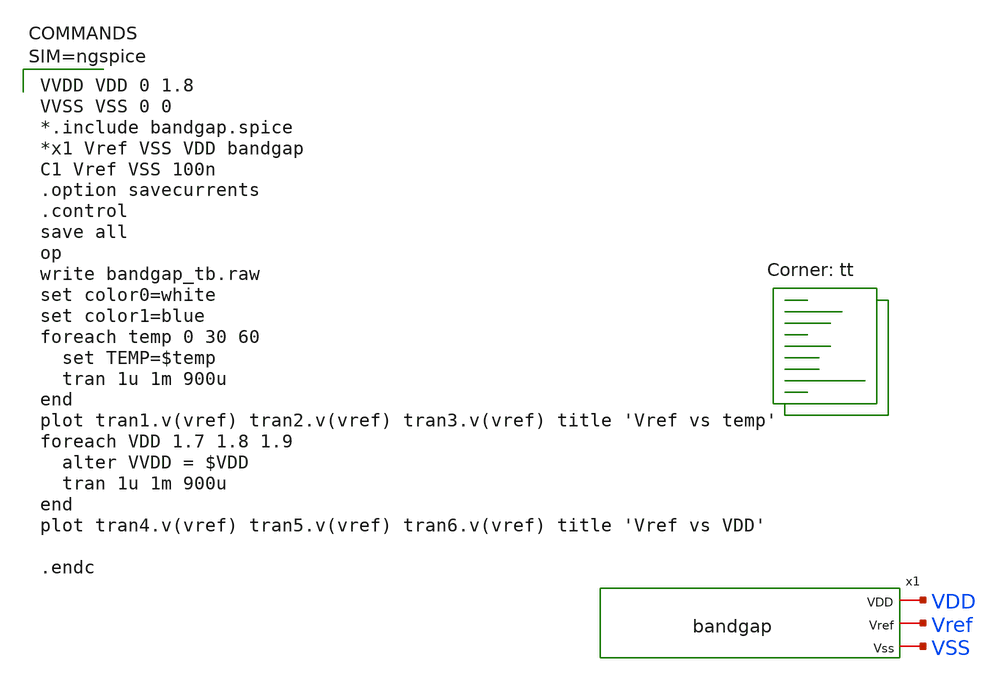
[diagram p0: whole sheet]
** sch_path: hw05/xschem/bandgap_tb.sch
**.subckt bandgap_tb
x1 VDD Vref VSS bandgap
**** begin user architecture code
.lib $::SKYWATER_MODELS/sky130.lib.spice tt


VVDD VDD 0 1.8
VVSS VSS 0 0
*.include bandgap.spice
*x1 Vref VSS VDD bandgap
C1 Vref VSS 100n
.option savecurrents
.control
save all
op
write bandgap_tb.raw
set color0=white
set color1=blue
foreach temp 0 30 60
  set TEMP=$temp
  tran 1u 1m 900u
end
plot tran1.v(vref) tran2.v(vref) tran3.v(vref) title 'Vref vs temp'
foreach VDD 1.7 1.8 1.9
  alter VVDD = $VDD
  tran 1u 1m 900u
end
plot tran4.v(vref) tran5.v(vref) tran6.v(vref) title 'Vref vs VDD'

.endc



**** end user architecture code
**.ends

* expanding   symbol:  bandgap.sym # of pins=3
** sym_path: hw05/xschem/bandgap.sym
** sch_path: hw05/xschem/bandgap.sch
.subckt bandgap VDD Vref Vss
*.iopin VDD
*.iopin Vss
*.iopin Vref
XM7 net2 Vref net8 Vss sky130_fd_pr__nfet_01v8 L=1 W=20 nf=1 ad='int((nf+1)/2) * W/nf * 0.29' as='int((nf+2)/2) * W/nf * 0.29'
+ pd='2*int((nf+1)/2) * (W/nf + 0.29)' ps='2*int((nf+2)/2) * (W/nf + 0.29)' nrd='0.29 / W' nrs='0.29 / W'
+ sa=0 sb=0 sd=0 mult=1 m=1
XM1 net1 net1 VDD VDD sky130_fd_pr__pfet_01v8 L=1 W=1 nf=1 ad='int((nf+1)/2) * W/nf * 0.29' as='int((nf+2)/2) * W/nf * 0.29'
+ pd='2*int((nf+1)/2) * (W/nf + 0.29)' ps='2*int((nf+2)/2) * (W/nf + 0.29)' nrd='0.29 / W' nrs='0.29 / W'
+ sa=0 sb=0 sd=0 mult=1 m=1
XM2 net2 net1 VDD VDD sky130_fd_pr__pfet_01v8 L=1 W=1 nf=1 ad='int((nf+1)/2) * W/nf * 0.29' as='int((nf+2)/2) * W/nf * 0.29'
+ pd='2*int((nf+1)/2) * (W/nf + 0.29)' ps='2*int((nf+2)/2) * (W/nf + 0.29)' nrd='0.29 / W' nrs='0.29 / W'
+ sa=0 sb=0 sd=0 mult=1 m=1
XM3 net5 net1 VDD VDD sky130_fd_pr__pfet_01v8 L=1 W=1 nf=1 ad='int((nf+1)/2) * W/nf * 0.29' as='int((nf+2)/2) * W/nf * 0.29'
+ pd='2*int((nf+1)/2) * (W/nf + 0.29)' ps='2*int((nf+2)/2) * (W/nf + 0.29)' nrd='0.29 / W' nrs='0.29 / W'
+ sa=0 sb=0 sd=0 mult=1 m=1
XM4 Vref net2 VDD VDD sky130_fd_pr__pfet_01v8 L=.5 W=20 nf=1 ad='int((nf+1)/2) * W/nf * 0.29' as='int((nf+2)/2) * W/nf * 0.29'
+ pd='2*int((nf+1)/2) * (W/nf + 0.29)' ps='2*int((nf+2)/2) * (W/nf + 0.29)' nrd='0.29 / W' nrs='0.29 / W'
+ sa=0 sb=0 sd=0 mult=1 m=1
XM5 net1 Vref net4 Vss sky130_fd_pr__nfet_01v8 L=1 W=5 nf=1 ad='int((nf+1)/2) * W/nf * 0.29' as='int((nf+2)/2) * W/nf * 0.29'
+ pd='2*int((nf+1)/2) * (W/nf + 0.29)' ps='2*int((nf+2)/2) * (W/nf + 0.29)' nrd='0.29 / W' nrs='0.29 / W'
+ sa=0 sb=0 sd=0 mult=1 m=1
XR1 net3 net4 Vss sky130_fd_pr__res_xhigh_po_5p73 L=80 mult=1 m=1
XR2 Vss net3 Vss sky130_fd_pr__res_xhigh_po_5p73 L=80 mult=1 m=1
XM6 net9 net2 Vss Vss sky130_fd_pr__nfet_01v8 L=50 W=.42 nf=1 ad='int((nf+1)/2) * W/nf * 0.29' as='int((nf+2)/2) * W/nf * 0.29'
+ pd='2*int((nf+1)/2) * (W/nf + 0.29)' ps='2*int((nf+2)/2) * (W/nf + 0.29)' nrd='0.29 / W' nrs='0.29 / W'
+ sa=0 sb=0 sd=0 mult=1 m=1
XM8 net8 net7 Vss Vss sky130_fd_pr__nfet_01v8 L=1 W=20 nf=1 ad='int((nf+1)/2) * W/nf * 0.29' as='int((nf+2)/2) * W/nf * 0.29'
+ pd='2*int((nf+1)/2) * (W/nf + 0.29)' ps='2*int((nf+2)/2) * (W/nf + 0.29)' nrd='0.29 / W' nrs='0.29 / W'
+ sa=0 sb=0 sd=0 mult=1 m=1
XM9 net7 net6 Vss Vss sky130_fd_pr__nfet_01v8 L=1 W=20 nf=1 ad='int((nf+1)/2) * W/nf * 0.29' as='int((nf+2)/2) * W/nf * 0.29'
+ pd='2*int((nf+1)/2) * (W/nf + 0.29)' ps='2*int((nf+2)/2) * (W/nf + 0.29)' nrd='0.29 / W' nrs='0.29 / W'
+ sa=0 sb=0 sd=0 mult=1 m=1
XM10 net6 net6 Vss Vss sky130_fd_pr__nfet_01v8 L=1 W=20 nf=1 ad='int((nf+1)/2) * W/nf * 0.29' as='int((nf+2)/2) * W/nf * 0.29'
+ pd='2*int((nf+1)/2) * (W/nf + 0.29)' ps='2*int((nf+2)/2) * (W/nf + 0.29)' nrd='0.29 / W' nrs='0.29 / W'
+ sa=0 sb=0 sd=0 mult=1 m=1
XM11 net7 net10 net5 net5 sky130_fd_pr__pfet_01v8 L=1 W=20 nf=1 ad='int((nf+1)/2) * W/nf * 0.29' as='int((nf+2)/2) * W/nf * 0.29'
+ pd='2*int((nf+1)/2) * (W/nf + 0.29)' ps='2*int((nf+2)/2) * (W/nf + 0.29)' nrd='0.29 / W' nrs='0.29 / W'
+ sa=0 sb=0 sd=0 mult=1 m=1
XM12 net6 net12 net5 net5 sky130_fd_pr__pfet_01v8 L=1 W=20 nf=1 ad='int((nf+1)/2) * W/nf * 0.29' as='int((nf+2)/2) * W/nf * 0.29'
+ pd='2*int((nf+1)/2) * (W/nf + 0.29)' ps='2*int((nf+2)/2) * (W/nf + 0.29)' nrd='0.29 / W' nrs='0.29 / W'
+ sa=0 sb=0 sd=0 mult=1 m=1
XM13 net2 net2 net9 Vss sky130_fd_pr__nfet_01v8 L=50 W=.42 nf=1 ad='int((nf+1)/2) * W/nf * 0.29' as='int((nf+2)/2) * W/nf * 0.29'
+ pd='2*int((nf+1)/2) * (W/nf + 0.29)' ps='2*int((nf+2)/2) * (W/nf + 0.29)' nrd='0.29 / W' nrs='0.29 / W'
+ sa=0 sb=0 sd=0 mult=1 m=1
XR3 net10 Vref Vss sky130_fd_pr__res_xhigh_po_5p73 L=80 mult=1 m=1
XR4 net12 Vref Vss sky130_fd_pr__res_xhigh_po_5p73 L=80 mult=1 m=1
XR5 net11 net10 Vss sky130_fd_pr__res_xhigh_po_5p73 L=20 mult=1 m=1
XQ1 Vss Vss net12 sky130_fd_pr__pnp_05v5_W3p40L3p40 m=1
XQ2 Vss Vss net11 sky130_fd_pr__pnp_05v5_W3p40L3p40 m=24
.ends

.end
